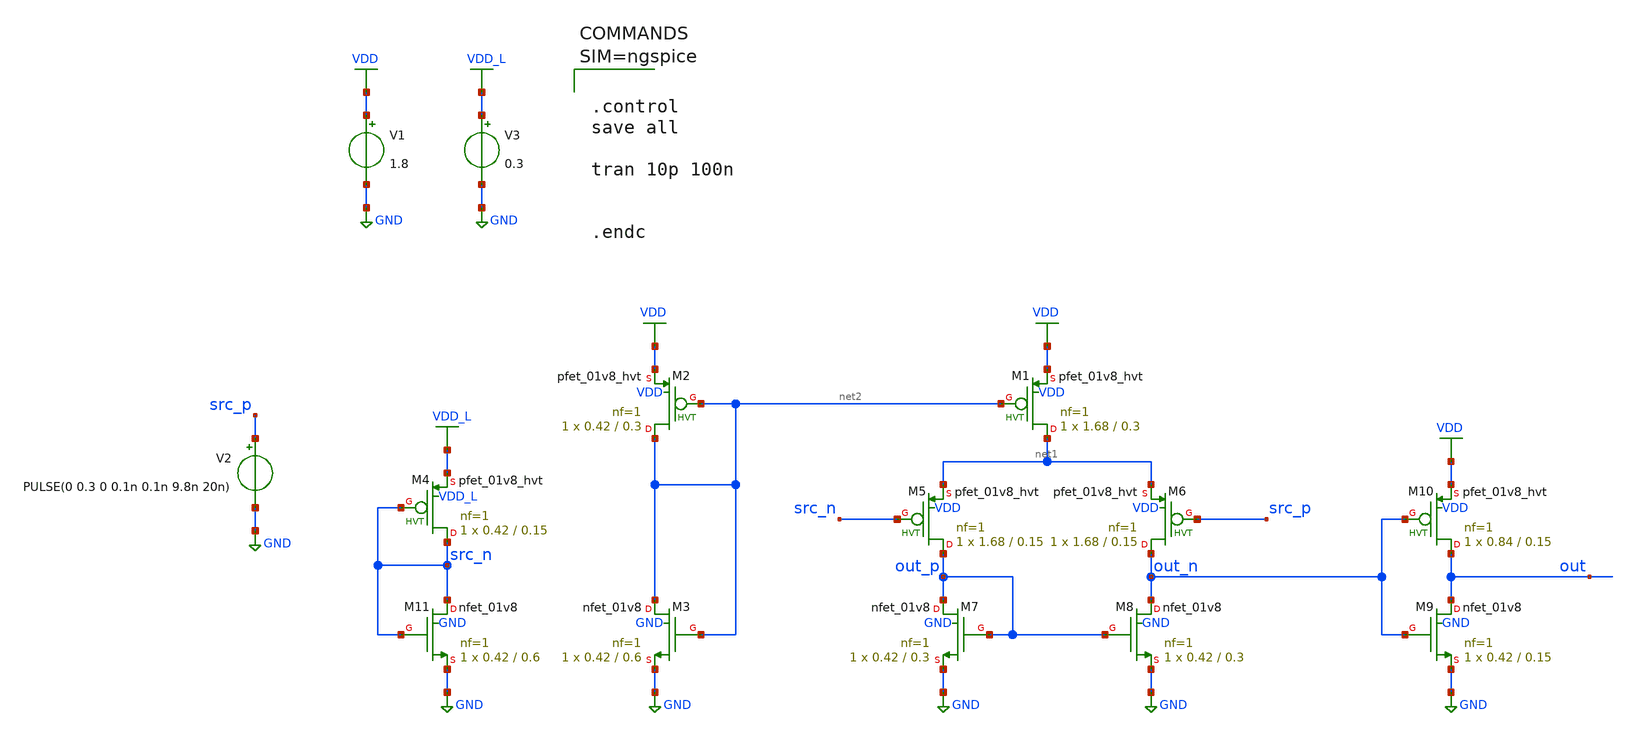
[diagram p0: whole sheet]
** sch_path: xschem/tb_lvl2.sch
**.subckt tb_lvl2
V1 VDD GND 1.8
V2 src_p GND PULSE(0 0.3 0 0.1n 0.1n 9.8n 20n)
V3 VDD_L GND 0.3
XM5 out_p src_n net1 VDD sky130_fd_pr__pfet_01v8_hvt L=0.15 W=1.68 nf=1 ad='int((nf+1)/2) * W/nf * 0.29'
+ as='int((nf+2)/2) * W/nf * 0.29' pd='2*int((nf+1)/2) * (W/nf + 0.29)' ps='2*int((nf+2)/2) * (W/nf + 0.29)'
+ nrd='0.29 / W' nrs='0.29 / W' sa=0 sb=0 sd=0 mult=1 m=1
XM6 out_n src_p net1 VDD sky130_fd_pr__pfet_01v8_hvt L=0.15 W=1.68 nf=1 ad='int((nf+1)/2) * W/nf * 0.29'
+ as='int((nf+2)/2) * W/nf * 0.29' pd='2*int((nf+1)/2) * (W/nf + 0.29)' ps='2*int((nf+2)/2) * (W/nf + 0.29)'
+ nrd='0.29 / W' nrs='0.29 / W' sa=0 sb=0 sd=0 mult=1 m=1
XM7 out_p out_p GND GND sky130_fd_pr__nfet_01v8 L=0.3 W=0.42 nf=1 ad='int((nf+1)/2) * W/nf * 0.29' as='int((nf+2)/2) * W/nf * 0.29'
+ pd='2*int((nf+1)/2) * (W/nf + 0.29)' ps='2*int((nf+2)/2) * (W/nf + 0.29)' nrd='0.29 / W' nrs='0.29 / W'
+ sa=0 sb=0 sd=0 mult=1 m=1
XM8 out_n out_p GND GND sky130_fd_pr__nfet_01v8 L=0.3 W=0.42 nf=1 ad='int((nf+1)/2) * W/nf * 0.29' as='int((nf+2)/2) * W/nf * 0.29'
+ pd='2*int((nf+1)/2) * (W/nf + 0.29)' ps='2*int((nf+2)/2) * (W/nf + 0.29)' nrd='0.29 / W' nrs='0.29 / W'
+ sa=0 sb=0 sd=0 mult=1 m=1
XM9 out out_n GND GND sky130_fd_pr__nfet_01v8 L=0.15 W=0.42 nf=1 ad='int((nf+1)/2) * W/nf * 0.29' as='int((nf+2)/2) * W/nf * 0.29'
+ pd='2*int((nf+1)/2) * (W/nf + 0.29)' ps='2*int((nf+2)/2) * (W/nf + 0.29)' nrd='0.29 / W' nrs='0.29 / W'
+ sa=0 sb=0 sd=0 mult=1 m=1
XM10 out out_n VDD VDD sky130_fd_pr__pfet_01v8_hvt L=0.15 W=0.84 nf=1 ad='int((nf+1)/2) * W/nf * 0.29'
+ as='int((nf+2)/2) * W/nf * 0.29' pd='2*int((nf+1)/2) * (W/nf + 0.29)' ps='2*int((nf+2)/2) * (W/nf + 0.29)'
+ nrd='0.29 / W' nrs='0.29 / W' sa=0 sb=0 sd=0 mult=1 m=1
XM1 net1 net2 VDD VDD sky130_fd_pr__pfet_01v8_hvt L=0.3 W=1.68 nf=1 ad='int((nf+1)/2) * W/nf * 0.29'
+ as='int((nf+2)/2) * W/nf * 0.29' pd='2*int((nf+1)/2) * (W/nf + 0.29)' ps='2*int((nf+2)/2) * (W/nf + 0.29)'
+ nrd='0.29 / W' nrs='0.29 / W' sa=0 sb=0 sd=0 mult=1 m=1
XM2 net2 net2 VDD VDD sky130_fd_pr__pfet_01v8_hvt L=0.3 W=0.42 nf=1 ad='int((nf+1)/2) * W/nf * 0.29'
+ as='int((nf+2)/2) * W/nf * 0.29' pd='2*int((nf+1)/2) * (W/nf + 0.29)' ps='2*int((nf+2)/2) * (W/nf + 0.29)'
+ nrd='0.29 / W' nrs='0.29 / W' sa=0 sb=0 sd=0 mult=1 m=1
XM3 net2 net2 GND GND sky130_fd_pr__nfet_01v8 L=0.6 W=0.42 nf=1 ad='int((nf+1)/2) * W/nf * 0.29' as='int((nf+2)/2) * W/nf * 0.29'
+ pd='2*int((nf+1)/2) * (W/nf + 0.29)' ps='2*int((nf+2)/2) * (W/nf + 0.29)' nrd='0.29 / W' nrs='0.29 / W'
+ sa=0 sb=0 sd=0 mult=1 m=1
XM4 src_n src_n VDD_L VDD_L sky130_fd_pr__pfet_01v8_hvt L=0.15 W=0.42 nf=1 ad='int((nf+1)/2) * W/nf * 0.29'
+ as='int((nf+2)/2) * W/nf * 0.29' pd='2*int((nf+1)/2) * (W/nf + 0.29)' ps='2*int((nf+2)/2) * (W/nf + 0.29)'
+ nrd='0.29 / W' nrs='0.29 / W' sa=0 sb=0 sd=0 mult=1 m=1
XM11 src_n src_n GND GND sky130_fd_pr__nfet_01v8 L=0.6 W=0.42 nf=1 ad='int((nf+1)/2) * W/nf * 0.29' as='int((nf+2)/2) * W/nf * 0.29'
+ pd='2*int((nf+1)/2) * (W/nf + 0.29)' ps='2*int((nf+2)/2) * (W/nf + 0.29)' nrd='0.29 / W' nrs='0.29 / W'
+ sa=0 sb=0 sd=0 mult=1 m=1
**** begin user architecture code

** opencircuitdesign pdks install
.lib $::SKYWATER_MODELS/sky130.lib.spice ff
.include $::SKYWATER_STDCELLS/sky130_fd_sc_hd.spice
.param mc_mm_switch=0
.option wnflag=1




.control
save all

tran 10p 100n


.endc



**** end user architecture code
**.ends
.GLOBAL GND
.GLOBAL VDD
.GLOBAL VDD_L
.end
